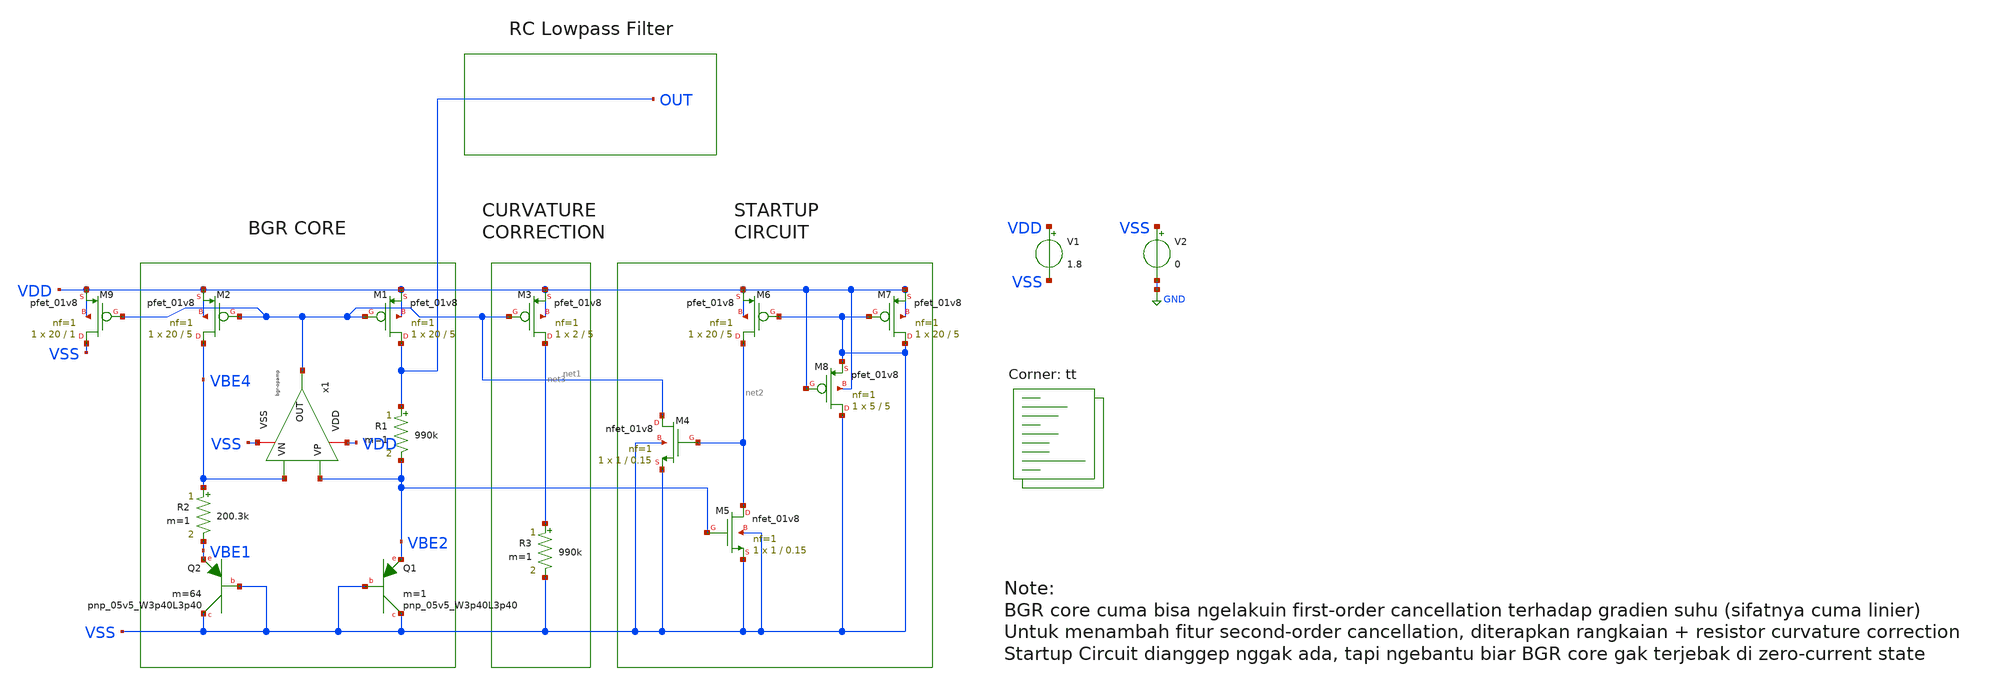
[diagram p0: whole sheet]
** sch_path: bandgap/bgr2.sch
**.subckt bgr2
XM1 OUT net1 VDD VDD sky130_fd_pr__pfet_01v8 L=5 W=20 nf=1 ad='int((nf+1)/2) * W/nf * 0.29' as='int((nf+2)/2) * W/nf * 0.29'
+ pd='2*int((nf+1)/2) * (W/nf + 0.29)' ps='2*int((nf+2)/2) * (W/nf + 0.29)' nrd='0.29 / W' nrs='0.29 / W'
+ sa=0 sb=0 sd=0 mult=1 m=1
XM2 VBE4 net1 VDD VDD sky130_fd_pr__pfet_01v8 L=5 W=20 nf=1 ad='int((nf+1)/2) * W/nf * 0.29' as='int((nf+2)/2) * W/nf * 0.29'
+ pd='2*int((nf+1)/2) * (W/nf + 0.29)' ps='2*int((nf+2)/2) * (W/nf + 0.29)' nrd='0.29 / W' nrs='0.29 / W'
+ sa=0 sb=0 sd=0 mult=1 m=1
R1 OUT VBE2 990k m=1
R2 VBE4 VBE1 200.3k m=1
XQ1 VSS VSS VBE2 sky130_fd_pr__pnp_05v5_W3p40L3p40 m=1
XQ2 VSS VSS VBE1 sky130_fd_pr__pnp_05v5_W3p40L3p40 m=64
V1 VDD VSS 1.8
V2 VSS GND 0
XM3 net3 net1 VDD VDD sky130_fd_pr__pfet_01v8 L=5 W=2 nf=1 ad='int((nf+1)/2) * W/nf * 0.29' as='int((nf+2)/2) * W/nf * 0.29'
+ pd='2*int((nf+1)/2) * (W/nf + 0.29)' ps='2*int((nf+2)/2) * (W/nf + 0.29)' nrd='0.29 / W' nrs='0.29 / W'
+ sa=0 sb=0 sd=0 mult=1 m=1
XM4 net1 net2 VSS VSS sky130_fd_pr__nfet_01v8 L=0.15 W=1 nf=1 ad='int((nf+1)/2) * W/nf * 0.29' as='int((nf+2)/2) * W/nf * 0.29'
+ pd='2*int((nf+1)/2) * (W/nf + 0.29)' ps='2*int((nf+2)/2) * (W/nf + 0.29)' nrd='0.29 / W' nrs='0.29 / W'
+ sa=0 sb=0 sd=0 mult=1 m=1
XM5 net2 VBE2 VSS VSS sky130_fd_pr__nfet_01v8 L=0.15 W=1 nf=1 ad='int((nf+1)/2) * W/nf * 0.29' as='int((nf+2)/2) * W/nf * 0.29'
+ pd='2*int((nf+1)/2) * (W/nf + 0.29)' ps='2*int((nf+2)/2) * (W/nf + 0.29)' nrd='0.29 / W' nrs='0.29 / W'
+ sa=0 sb=0 sd=0 mult=1 m=1
XM6 net2 VSS VDD VDD sky130_fd_pr__pfet_01v8 L=5 W=20 nf=1 ad='int((nf+1)/2) * W/nf * 0.29' as='int((nf+2)/2) * W/nf * 0.29'
+ pd='2*int((nf+1)/2) * (W/nf + 0.29)' ps='2*int((nf+2)/2) * (W/nf + 0.29)' nrd='0.29 / W' nrs='0.29 / W'
+ sa=0 sb=0 sd=0 mult=1 m=1
XM7 VSS VSS VDD VDD sky130_fd_pr__pfet_01v8 L=5 W=20 nf=1 ad='int((nf+1)/2) * W/nf * 0.29' as='int((nf+2)/2) * W/nf * 0.29'
+ pd='2*int((nf+1)/2) * (W/nf + 0.29)' ps='2*int((nf+2)/2) * (W/nf + 0.29)' nrd='0.29 / W' nrs='0.29 / W'
+ sa=0 sb=0 sd=0 mult=1 m=1
XM8 VSS VDD VSS VDD sky130_fd_pr__pfet_01v8 L=5 W=5 nf=1 ad='int((nf+1)/2) * W/nf * 0.29' as='int((nf+2)/2) * W/nf * 0.29'
+ pd='2*int((nf+1)/2) * (W/nf + 0.29)' ps='2*int((nf+2)/2) * (W/nf + 0.29)' nrd='0.29 / W' nrs='0.29 / W'
+ sa=0 sb=0 sd=0 mult=1 m=1
R3 net3 VSS 990k m=1
x1 VDD net1 VBE2 VBE4 VSS bgr-opamp
XM9 VSS net1 VDD VDD sky130_fd_pr__pfet_01v8 L=1 W=20 nf=1 ad='int((nf+1)/2) * W/nf * 0.29' as='int((nf+2)/2) * W/nf * 0.29'
+ pd='2*int((nf+1)/2) * (W/nf + 0.29)' ps='2*int((nf+2)/2) * (W/nf + 0.29)' nrd='0.29 / W' nrs='0.29 / W'
+ sa=0 sb=0 sd=0 mult=1 m=1
**** begin user architecture code
.lib $::SKYWATER_MODELS/sky130.lib.spice tt



.temp 125
.control
 DC v1 1.62 1.98 0.0001
 plot OUT2
 let PTAT = 4.94*(VBE2 - VBE1)
 let CC = 4.94*(VBE5)
 let CTAT = VBE1
 let VREF = PTAT + CTAT + CC
 let Verr = VREF - OUT
 let pwr = -i(V1)*1.8
 Bcorr VREF_CORR 0 V = V(VREF_RAW) - (1.26596064e-2 + (-5.94362766e-7)*(temp-27) +
+ (-5.24694018e-7)*pwr(temp-27,2) + (2.27088537e-9)*pwr(temp-27,3))
 plot V(VREF_CORR)
 plot i(Vmeas)
 plot pwr
 plot OUT PTAT CTAT
 plot OUT VDD
 plot VREF
 plot VERR
 plot VREF - VERR()


.endc


**** end user architecture code
**.ends

* expanding   symbol:  /foss/designs/afe-icdec-teknofest-2026/bandgap/bgr-opamp/bgr-opamp.sym # of
*+ pins=5
** sym_path: bandgap/bgr-opamp/bgr-opamp.sym
** sch_path: bandgap/bgr-opamp/bgr-opamp.sch
.subckt bgr-opamp VDD OUT VP VN VSS
*.iopin VSS
*.iopin VDD
*.ipin VP
*.ipin VN
*.opin OUT
XM1 net1 VP net3 VSS sky130_fd_pr__nfet_01v8 L=0.3 W=2.5 nf=2 ad='int((nf+1)/2) * W/nf * 0.29' as='int((nf+2)/2) * W/nf * 0.29'
+ pd='2*int((nf+1)/2) * (W/nf + 0.29)' ps='2*int((nf+2)/2) * (W/nf + 0.29)' nrd='0.29 / W' nrs='0.29 / W'
+ sa=0 sb=0 sd=0 mult=1 m=1
XM2 net2 VN net3 VSS sky130_fd_pr__nfet_01v8 L=0.3 W=2.5 nf=2 ad='int((nf+1)/2) * W/nf * 0.29' as='int((nf+2)/2) * W/nf * 0.29'
+ pd='2*int((nf+1)/2) * (W/nf + 0.29)' ps='2*int((nf+2)/2) * (W/nf + 0.29)' nrd='0.29 / W' nrs='0.29 / W'
+ sa=0 sb=0 sd=0 mult=1 m=1
XM4 net2 net1 VDD VDD sky130_fd_pr__pfet_01v8 L=1.25 W=10.8 nf=4 ad='int((nf+1)/2) * W/nf * 0.29' as='int((nf+2)/2) * W/nf * 0.29'
+ pd='2*int((nf+1)/2) * (W/nf + 0.29)' ps='2*int((nf+2)/2) * (W/nf + 0.29)' nrd='0.29 / W' nrs='0.29 / W'
+ sa=0 sb=0 sd=0 mult=1 m=1
XM3 net1 net1 VDD VDD sky130_fd_pr__pfet_01v8 L=1.25 W=10.8 nf=4 ad='int((nf+1)/2) * W/nf * 0.29' as='int((nf+2)/2) * W/nf * 0.29'
+ pd='2*int((nf+1)/2) * (W/nf + 0.29)' ps='2*int((nf+2)/2) * (W/nf + 0.29)' nrd='0.29 / W' nrs='0.29 / W'
+ sa=0 sb=0 sd=0 mult=1 m=1
XM5 net3 net4 VSS VSS sky130_fd_pr__nfet_01v8 L=1.25 W=3.4 nf=1 ad='int((nf+1)/2) * W/nf * 0.29' as='int((nf+2)/2) * W/nf * 0.29'
+ pd='2*int((nf+1)/2) * (W/nf + 0.29)' ps='2*int((nf+2)/2) * (W/nf + 0.29)' nrd='0.29 / W' nrs='0.29 / W'
+ sa=0 sb=0 sd=0 mult=1 m=1
XM9 net4 net5 net10 VSS sky130_fd_pr__nfet_01v8 L=1.25 W=3.4 nf=1 ad='int((nf+1)/2) * W/nf * 0.29' as='int((nf+2)/2) * W/nf * 0.29'
+ pd='2*int((nf+1)/2) * (W/nf + 0.29)' ps='2*int((nf+2)/2) * (W/nf + 0.29)' nrd='0.29 / W' nrs='0.29 / W'
+ sa=0 sb=0 sd=0 mult=1 m=1
XM8 net4 net4 VDD VDD sky130_fd_pr__pfet_01v8 L=1.25 W=10.8 nf=4 ad='int((nf+1)/2) * W/nf * 0.29' as='int((nf+2)/2) * W/nf * 0.29'
+ pd='2*int((nf+1)/2) * (W/nf + 0.29)' ps='2*int((nf+2)/2) * (W/nf + 0.29)' nrd='0.29 / W' nrs='0.29 / W'
+ sa=0 sb=0 sd=0 mult=1 m=1
XM11 net5 net4 VDD VDD sky130_fd_pr__pfet_01v8 L=1.25 W=10.8 nf=4 ad='int((nf+1)/2) * W/nf * 0.29' as='int((nf+2)/2) * W/nf * 0.29'
+ pd='2*int((nf+1)/2) * (W/nf + 0.29)' ps='2*int((nf+2)/2) * (W/nf + 0.29)' nrd='0.29 / W' nrs='0.29 / W'
+ sa=0 sb=0 sd=0 mult=1 m=1
XM10 net5 net5 VSS VSS sky130_fd_pr__nfet_01v8 L=1.25 W=3.4 nf=1 ad='int((nf+1)/2) * W/nf * 0.29' as='int((nf+2)/2) * W/nf * 0.29'
+ pd='2*int((nf+1)/2) * (W/nf + 0.29)' ps='2*int((nf+2)/2) * (W/nf + 0.29)' nrd='0.29 / W' nrs='0.29 / W'
+ sa=0 sb=0 sd=0 mult=1 m=1
XM6 OUT net2 VDD VDD sky130_fd_pr__pfet_01v8 L=1.25 W=110 nf=32 ad='int((nf+1)/2) * W/nf * 0.29' as='int((nf+2)/2) * W/nf * 0.29'
+ pd='2*int((nf+1)/2) * (W/nf + 0.29)' ps='2*int((nf+2)/2) * (W/nf + 0.29)' nrd='0.29 / W' nrs='0.29 / W'
+ sa=0 sb=0 sd=0 mult=1 m=1
XM7 OUT net4 VSS VSS sky130_fd_pr__nfet_01v8 L=1.25 W=12 nf=4 ad='int((nf+1)/2) * W/nf * 0.29' as='int((nf+2)/2) * W/nf * 0.29'
+ pd='2*int((nf+1)/2) * (W/nf + 0.29)' ps='2*int((nf+2)/2) * (W/nf + 0.29)' nrd='0.29 / W' nrs='0.29 / W'
+ sa=0 sb=0 sd=0 mult=1 m=1
XC2 OUT net2 sky130_fd_pr__cap_mim_m3_1 W=15 L=15 MF=4 m=4
XM12 net4 net4 net5 VSS sky130_fd_pr__nfet_01v8 L=0.15 W=0.85 nf=1 ad='int((nf+1)/2) * W/nf * 0.29' as='int((nf+2)/2) * W/nf * 0.29'
+ pd='2*int((nf+1)/2) * (W/nf + 0.29)' ps='2*int((nf+2)/2) * (W/nf + 0.29)' nrd='0.29 / W' nrs='0.29 / W'
+ sa=0 sb=0 sd=0 mult=1 m=1
XR2 net6 net10 VSS sky130_fd_pr__res_high_po_1p41 L=3.235 mult=1 m=1
XR3 net8 net6 VSS sky130_fd_pr__res_high_po_1p41 L=3.235 mult=1 m=1
XR4 net7 net8 VSS sky130_fd_pr__res_high_po_1p41 L=3.235 mult=1 m=1
XR5 net9 net7 VSS sky130_fd_pr__res_high_po_1p41 L=3.235 mult=1 m=1
XR6 VSS net9 VSS sky130_fd_pr__res_high_po_1p41 L=3.235 mult=1 m=1
.ends

.GLOBAL GND
.end
